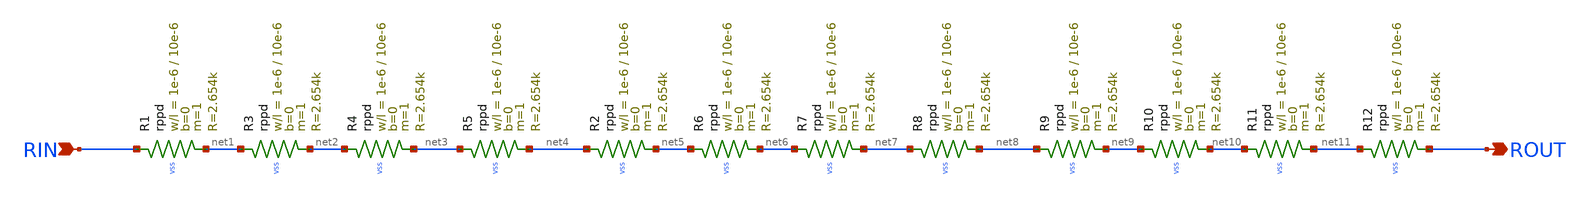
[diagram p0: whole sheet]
** sch_path: unic_cass_wrapper_analog/QDLL/Cells/RES.sch
**.subckt RES RIN ROUT
*.ipin RIN
*.opin ROUT
XR1 RIN net1 VSS rppd w=1e-6 l=10e-6 m=1 b=0 mm_ok=1
XR3 net1 net2 VSS rppd w=1e-6 l=10e-6 m=1 b=0 mm_ok=1
XR4 net2 net3 VSS rppd w=1e-6 l=10e-6 m=1 b=0 mm_ok=1
XR5 net3 net4 VSS rppd w=1e-6 l=10e-6 m=1 b=0 mm_ok=1
XR2 net4 net5 VSS rppd w=1e-6 l=10e-6 m=1 b=0 mm_ok=1
XR6 net5 net6 VSS rppd w=1e-6 l=10e-6 m=1 b=0 mm_ok=1
XR7 net6 net7 VSS rppd w=1e-6 l=10e-6 m=1 b=0 mm_ok=1
XR8 net7 net8 VSS rppd w=1e-6 l=10e-6 m=1 b=0 mm_ok=1
XR9 net8 net9 VSS rppd w=1e-6 l=10e-6 m=1 b=0 mm_ok=1
XR10 net9 net10 VSS rppd w=1e-6 l=10e-6 m=1 b=0 mm_ok=1
XR11 net10 net11 VSS rppd w=1e-6 l=10e-6 m=1 b=0 mm_ok=1
XR12 net11 ROUT VSS rppd w=1e-6 l=10e-6 m=1 b=0 mm_ok=1
**.ends
.end
